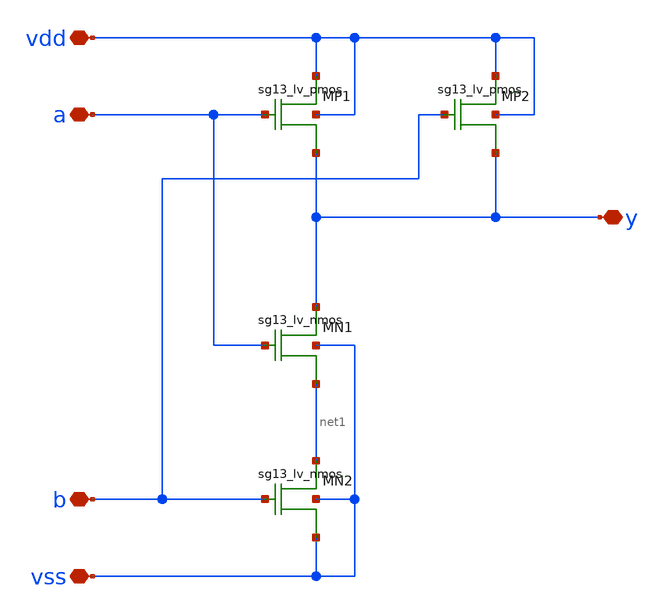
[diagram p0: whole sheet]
** sch_path: xschem/logic_gates/NANDLV.sch
**.subckt NANDLV vdd vss y a b
*.iopin vdd
*.iopin vss
*.iopin y
*.iopin a
*.iopin b
XMP1 vdd a y vdd sg13_lv_pmos w=1.0u l=0.13u ng=1 m=1
XMP2 vdd b y vdd sg13_lv_pmos w=1.0u l=0.13u ng=1 m=1
XMN1 y a net1 vss sg13_lv_nmos w=0.8u l=0.13u ng=1 m=1
XMN2 net1 b vss vss sg13_lv_nmos w=0.8u l=0.13u ng=1 m=1
**.ends
.end
